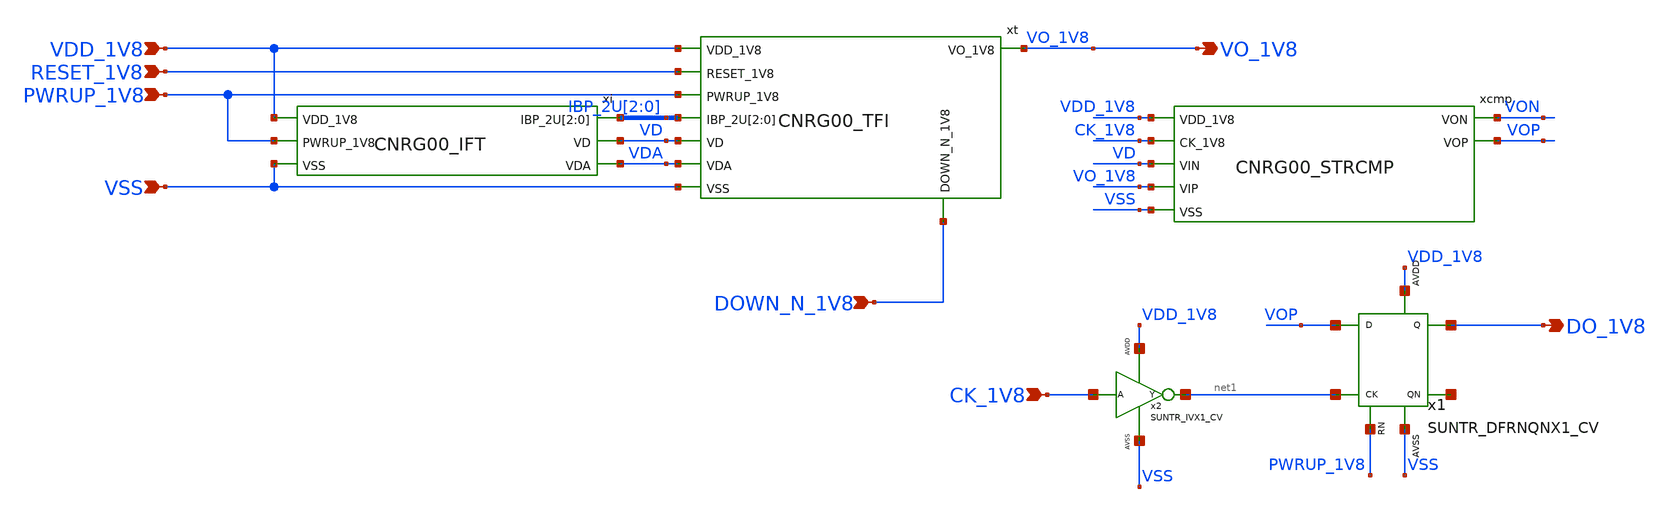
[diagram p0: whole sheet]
** sch_path: design/CNR_GR00_SKY130NM/CNR_GR00.sch
**.subckt CNR_GR00 VDD_1V8 VSS PWRUP_1V8 RESET_1V8 VO_1V8 DOWN_N_1V8 CK_1V8 DO_1V8
*.ipin VDD_1V8
*.ipin VSS
*.ipin PWRUP_1V8
*.ipin RESET_1V8
*.opin VO_1V8
*.ipin DOWN_N_1V8
*.ipin CK_1V8
*.opin DO_1V8
xi VDD_1V8 IBP_2U[2] IBP_2U[1] IBP_2U[0] VD VDA PWRUP_1V8 VSS CNRG00_IFT
xt RESET_1V8 VDD_1V8 VD VO_1V8 PWRUP_1V8 VDA IBP_2U[2] IBP_2U[1] IBP_2U[0] VSS DOWN_N_1V8 CNRG00_TFI
x1 VOP net1 PWRUP_1V8 DO_1V8 net2 VDD_1V8 VSS SUNTR_DFRNQNX1_CV xoffset=0 yoffset=0 angle=0
xcmp VDD_1V8 CK_1V8 VON VOP VD VO_1V8 VSS CNRG00_STRCMP
x2 CK_1V8 net1 VDD_1V8 VSS SUNTR_IVX1_CV
**.ends
.end
